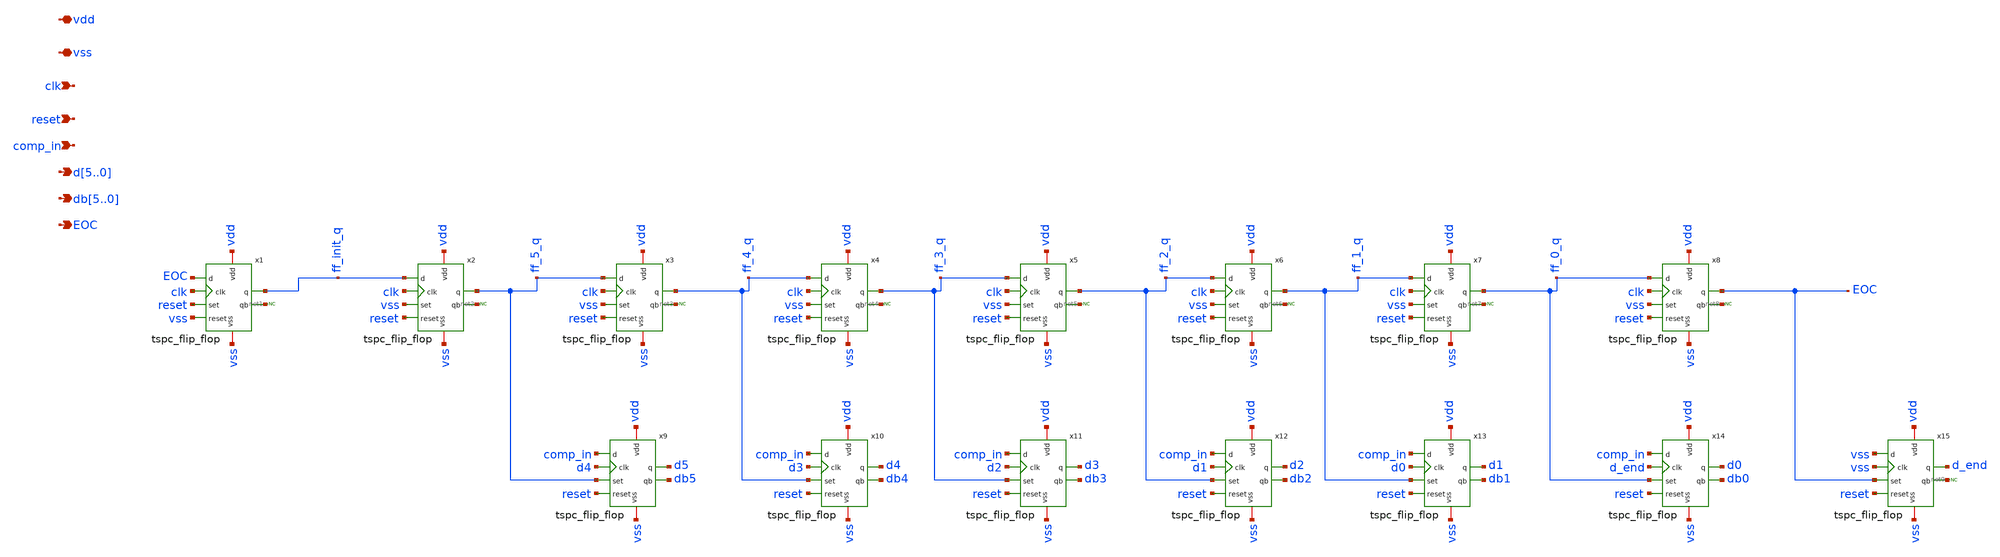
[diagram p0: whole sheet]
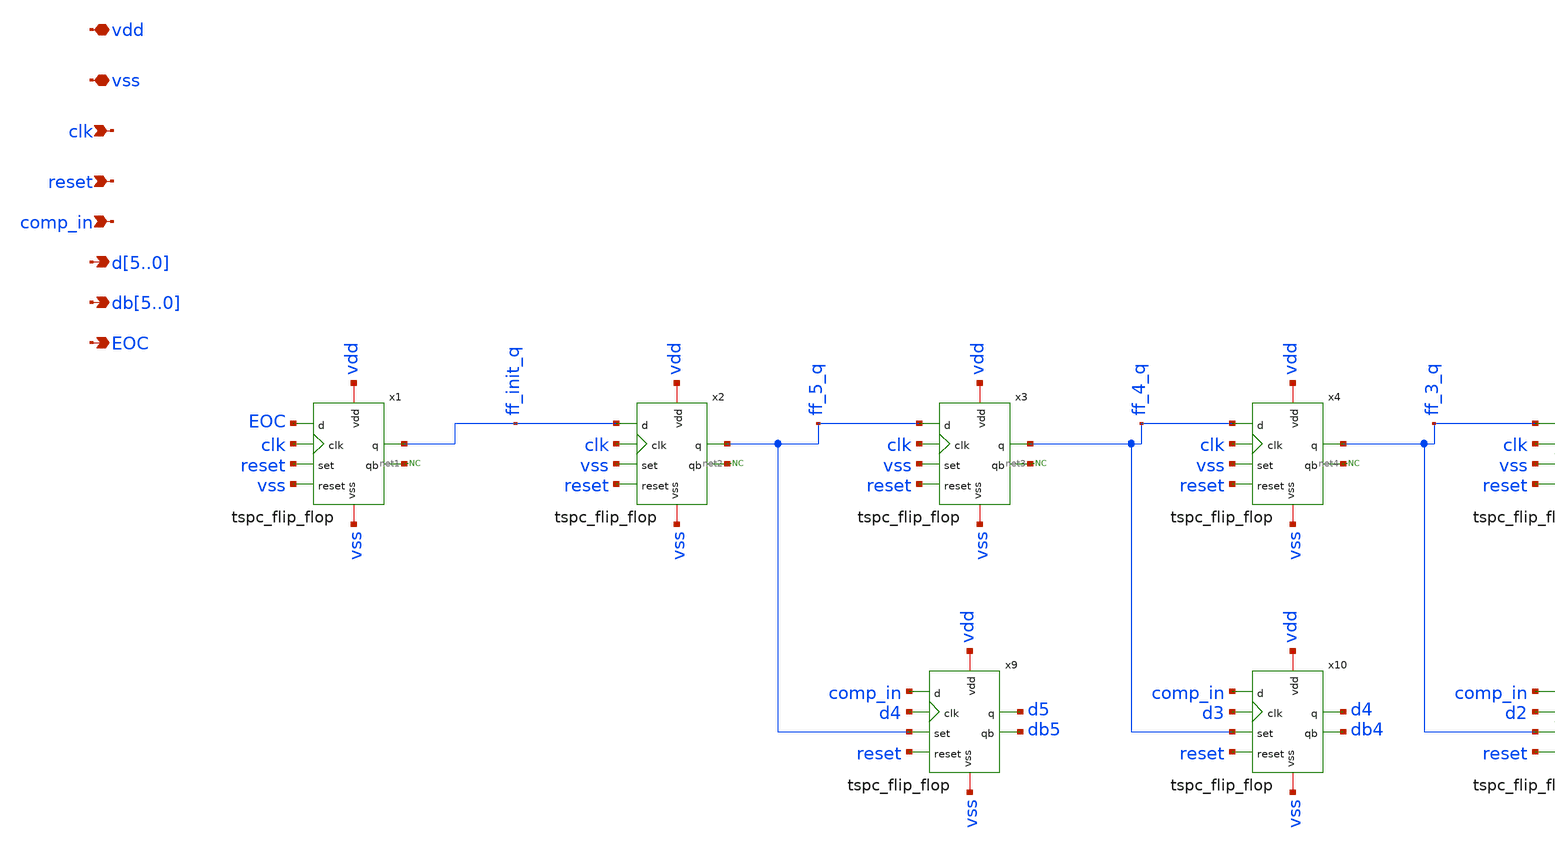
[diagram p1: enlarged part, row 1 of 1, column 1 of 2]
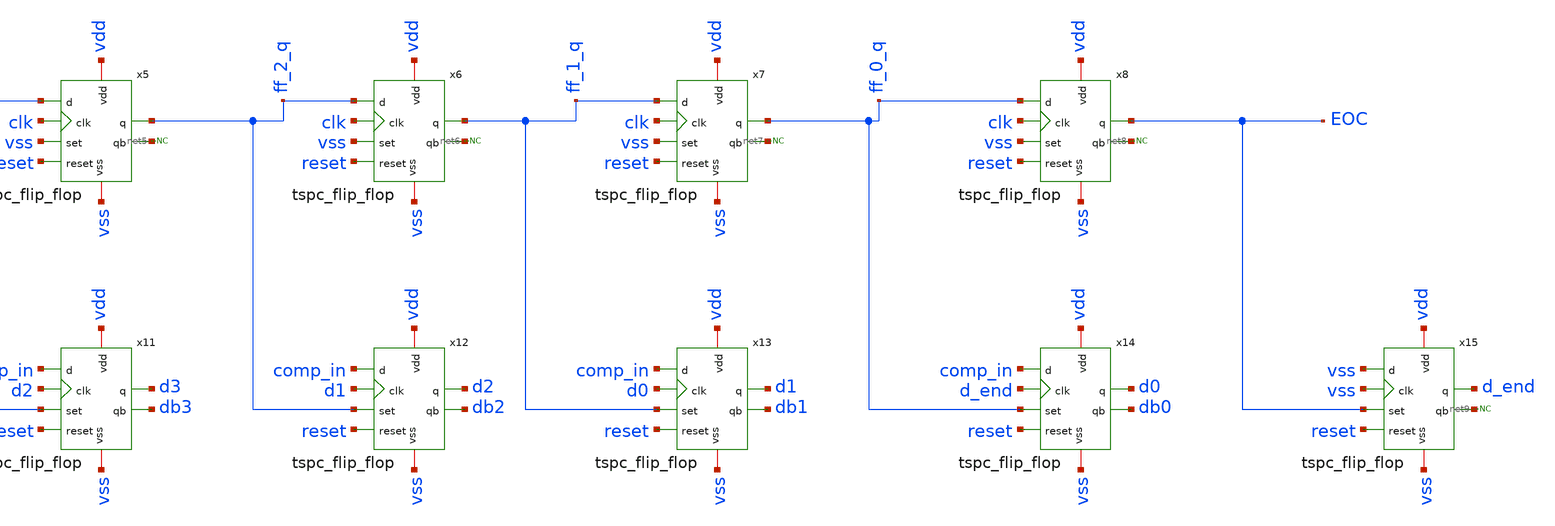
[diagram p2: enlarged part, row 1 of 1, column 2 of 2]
** sch_path: designs/libs/SAR_logic/SARlogicV2.sch
**.subckt SARlogicV2 comp_in vdd vss clk reset d5,d4,d3,d2,d1,d0 EOC db5,db4,db3,db2,db1,db0
*.ipin comp_in
*.iopin vdd
*.iopin vss
*.ipin clk
*.ipin reset
*.opin d5,d4,d3,d2,d1,d0
*.opin EOC
*.opin db5,db4,db3,db2,db1,db0
x1 vdd vss EOC clk reset vss ff_init_q net1 tspc_flip_flop
x2 vdd vss ff_init_q clk vss reset ff_5_q net2 tspc_flip_flop
x3 vdd vss ff_5_q clk vss reset ff_4_q net3 tspc_flip_flop
x4 vdd vss ff_4_q clk vss reset ff_3_q net4 tspc_flip_flop
x5 vdd vss ff_3_q clk vss reset ff_2_q net5 tspc_flip_flop
x6 vdd vss ff_2_q clk vss reset ff_1_q net6 tspc_flip_flop
x7 vdd vss ff_1_q clk vss reset ff_0_q net7 tspc_flip_flop
x8 vdd vss ff_0_q clk vss reset EOC net8 tspc_flip_flop
x9 vdd vss comp_in d4 ff_5_q reset d5 db5 tspc_flip_flop
x10 vdd vss comp_in d3 ff_4_q reset d4 db4 tspc_flip_flop
x11 vdd vss comp_in d2 ff_3_q reset d3 db3 tspc_flip_flop
x12 vdd vss comp_in d1 ff_2_q reset d2 db2 tspc_flip_flop
x13 vdd vss comp_in d0 ff_1_q reset d1 db1 tspc_flip_flop
x14 vdd vss comp_in d_end ff_0_q reset d0 db0 tspc_flip_flop
x15 vdd vss vss vss EOC reset d_end net9 tspc_flip_flop
* noconn #net2
* noconn #net3
* noconn #net4
* noconn #net5
* noconn #net6
* noconn #net7
* noconn #net8
* noconn #net9
* noconn #net1
**.ends

* expanding   symbol:  libs/tspc_flip_flop/tspc_flip_flop.sym # of pins=8
** sym_path: designs/libs/tspc_flip_flop/tspc_flip_flop.sym
** sch_path: designs/libs/tspc_flip_flop/tspc_flip_flop.sch
.subckt tspc_flip_flop vdd vss d clk set reset q qb
*.iopin vdd
*.iopin vss
*.ipin d
*.ipin clk
*.ipin set
*.ipin reset
*.opin q
*.opin qb
XM1 b1 d vss vss nfet_03v3 L=0.28u W=1u nf=1 ad='int((nf+1)/2) * W/nf * 0.18u' as='int((nf+2)/2) * W/nf * 0.18u'
+ pd='2*int((nf+1)/2) * (W/nf + 0.18u)' ps='2*int((nf+2)/2) * (W/nf + 0.18u)' nrd='0.18u / W' nrs='0.18u / W'
+ sa=0 sb=0 sd=0 m=1
XM2 b1 clk net1 net1 pfet_03v3 L=0.28u W=2u nf=1 ad='int((nf+1)/2) * W/nf * 0.18u' as='int((nf+2)/2) * W/nf * 0.18u'
+ pd='2*int((nf+1)/2) * (W/nf + 0.18u)' ps='2*int((nf+2)/2) * (W/nf + 0.18u)' nrd='0.18u / W' nrs='0.18u / W'
+ sa=0 sb=0 sd=0 m=1
XM3 net1 d vdd vdd pfet_03v3 L=0.28u W=2u nf=1 ad='int((nf+1)/2) * W/nf * 0.18u' as='int((nf+2)/2) * W/nf * 0.18u'
+ pd='2*int((nf+1)/2) * (W/nf + 0.18u)' ps='2*int((nf+2)/2) * (W/nf + 0.18u)' nrd='0.18u / W' nrs='0.18u / W'
+ sa=0 sb=0 sd=0 m=1
XM4 b2 clk vdd vdd pfet_03v3 L=0.28u W=2u nf=1 ad='int((nf+1)/2) * W/nf * 0.18u' as='int((nf+2)/2) * W/nf * 0.18u'
+ pd='2*int((nf+1)/2) * (W/nf + 0.18u)' ps='2*int((nf+2)/2) * (W/nf + 0.18u)' nrd='0.18u / W' nrs='0.18u / W'
+ sa=0 sb=0 sd=0 m=1
XM5 b2 b1 net2 vss nfet_03v3 L=0.28u W=1u nf=1 ad='int((nf+1)/2) * W/nf * 0.18u' as='int((nf+2)/2) * W/nf * 0.18u'
+ pd='2*int((nf+1)/2) * (W/nf + 0.18u)' ps='2*int((nf+2)/2) * (W/nf + 0.18u)' nrd='0.18u / W' nrs='0.18u / W'
+ sa=0 sb=0 sd=0 m=1
XM6 net2 clk vss vss nfet_03v3 L=0.28u W=1u nf=1 ad='int((nf+1)/2) * W/nf * 0.18u' as='int((nf+2)/2) * W/nf * 0.18u'
+ pd='2*int((nf+1)/2) * (W/nf + 0.18u)' ps='2*int((nf+2)/2) * (W/nf + 0.18u)' nrd='0.18u / W' nrs='0.18u / W'
+ sa=0 sb=0 sd=0 m=1
XM7 net4 b2 vss vss nfet_03v3 L=0.28u W=1u nf=1 ad='int((nf+1)/2) * W/nf * 0.18u' as='int((nf+2)/2) * W/nf * 0.18u'
+ pd='2*int((nf+1)/2) * (W/nf + 0.18u)' ps='2*int((nf+2)/2) * (W/nf + 0.18u)' nrd='0.18u / W' nrs='0.18u / W'
+ sa=0 sb=0 sd=0 m=1
XM8 b3 clk net4 vss nfet_03v3 L=0.28u W=1u nf=1 ad='int((nf+1)/2) * W/nf * 0.18u' as='int((nf+2)/2) * W/nf * 0.18u'
+ pd='2*int((nf+1)/2) * (W/nf + 0.18u)' ps='2*int((nf+2)/2) * (W/nf + 0.18u)' nrd='0.18u / W' nrs='0.18u / W'
+ sa=0 sb=0 sd=0 m=1
XM9 b3 set net3 net3 pfet_03v3 L=0.28u W=2u nf=1 ad='int((nf+1)/2) * W/nf * 0.18u' as='int((nf+2)/2) * W/nf * 0.18u'
+ pd='2*int((nf+1)/2) * (W/nf + 0.18u)' ps='2*int((nf+2)/2) * (W/nf + 0.18u)' nrd='0.18u / W' nrs='0.18u / W'
+ sa=0 sb=0 sd=0 m=1
XM10 net3 b2 vdd vdd pfet_03v3 L=0.28u W=2u nf=1 ad='int((nf+1)/2) * W/nf * 0.18u' as='int((nf+2)/2) * W/nf * 0.18u'
+ pd='2*int((nf+1)/2) * (W/nf + 0.18u)' ps='2*int((nf+2)/2) * (W/nf + 0.18u)' nrd='0.18u / W' nrs='0.18u / W'
+ sa=0 sb=0 sd=0 m=1
XM11 b3 net5 vdd vdd pfet_03v3 L=0.28u W=2u nf=1 ad='int((nf+1)/2) * W/nf * 0.18u' as='int((nf+2)/2) * W/nf * 0.18u'
+ pd='2*int((nf+1)/2) * (W/nf + 0.18u)' ps='2*int((nf+2)/2) * (W/nf + 0.18u)' nrd='0.18u / W' nrs='0.18u / W'
+ sa=0 sb=0 sd=0 m=1
XM12 b3 set vss vss nfet_03v3 L=0.28u W=1u nf=1 ad='int((nf+1)/2) * W/nf * 0.18u' as='int((nf+2)/2) * W/nf * 0.18u'
+ pd='2*int((nf+1)/2) * (W/nf + 0.18u)' ps='2*int((nf+2)/2) * (W/nf + 0.18u)' nrd='0.18u / W' nrs='0.18u / W'
+ sa=0 sb=0 sd=0 m=1
XM13 q b3 vdd vdd pfet_03v3 L=0.28u W=2u nf=1 ad='int((nf+1)/2) * W/nf * 0.18u' as='int((nf+2)/2) * W/nf * 0.18u'
+ pd='2*int((nf+1)/2) * (W/nf + 0.18u)' ps='2*int((nf+2)/2) * (W/nf + 0.18u)' nrd='0.18u / W' nrs='0.18u / W'
+ sa=0 sb=0 sd=0 m=1
XM14 q b3 vss vss nfet_03v3 L=0.28u W=1u nf=1 ad='int((nf+1)/2) * W/nf * 0.18u' as='int((nf+2)/2) * W/nf * 0.18u'
+ pd='2*int((nf+1)/2) * (W/nf + 0.18u)' ps='2*int((nf+2)/2) * (W/nf + 0.18u)' nrd='0.18u / W' nrs='0.18u / W'
+ sa=0 sb=0 sd=0 m=1
XM15 net5 reset vdd vdd pfet_03v3 L=0.28u W=2u nf=1 ad='int((nf+1)/2) * W/nf * 0.18u' as='int((nf+2)/2) * W/nf * 0.18u'
+ pd='2*int((nf+1)/2) * (W/nf + 0.18u)' ps='2*int((nf+2)/2) * (W/nf + 0.18u)' nrd='0.18u / W' nrs='0.18u / W'
+ sa=0 sb=0 sd=0 m=1
XM16 net5 reset vss vss nfet_03v3 L=0.28u W=1u nf=1 ad='int((nf+1)/2) * W/nf * 0.18u' as='int((nf+2)/2) * W/nf * 0.18u'
+ pd='2*int((nf+1)/2) * (W/nf + 0.18u)' ps='2*int((nf+2)/2) * (W/nf + 0.18u)' nrd='0.18u / W' nrs='0.18u / W'
+ sa=0 sb=0 sd=0 m=1
XM17 qb q vdd vdd pfet_03v3 L=0.28u W=2u nf=1 ad='int((nf+1)/2) * W/nf * 0.18u' as='int((nf+2)/2) * W/nf * 0.18u'
+ pd='2*int((nf+1)/2) * (W/nf + 0.18u)' ps='2*int((nf+2)/2) * (W/nf + 0.18u)' nrd='0.18u / W' nrs='0.18u / W'
+ sa=0 sb=0 sd=0 m=1
XM18 qb q vss vss nfet_03v3 L=0.28u W=1u nf=1 ad='int((nf+1)/2) * W/nf * 0.18u' as='int((nf+2)/2) * W/nf * 0.18u'
+ pd='2*int((nf+1)/2) * (W/nf + 0.18u)' ps='2*int((nf+2)/2) * (W/nf + 0.18u)' nrd='0.18u / W' nrs='0.18u / W'
+ sa=0 sb=0 sd=0 m=1
.ends

.end
